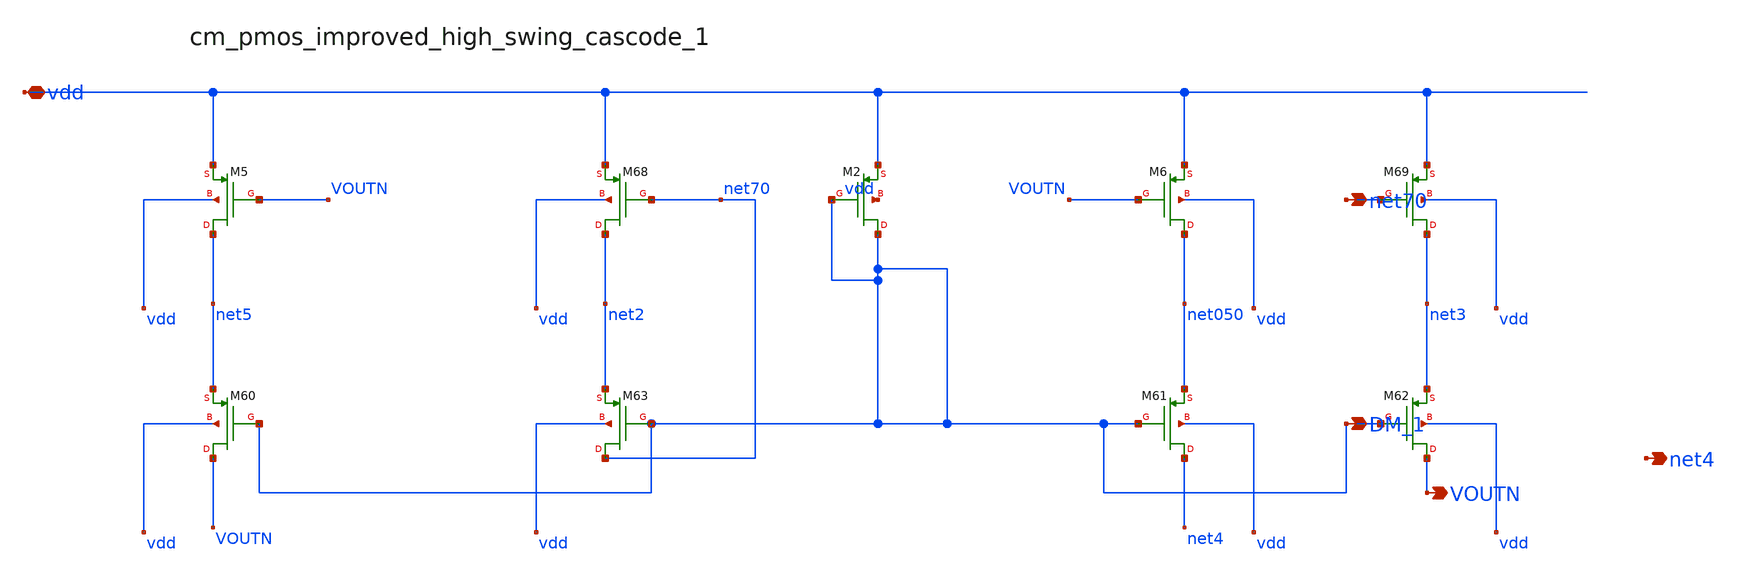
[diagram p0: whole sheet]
** sch_path: analog-db/raw/amp_016_song_dacfc/hier/blocks/cm_pmos_improved_high_swing_cascode_1.sch
**.subckt cm_pmos_improved_high_swing_cascode_1 vdd VOUTN net70 DM_1 net4
*.iopin vdd
*.opin VOUTN
*.opin net70
*.opin DM_1
*.opin net4
XM2 DM_1 DM_1 vdd vdd sg13_lv_pmos w=x_dut_xm2_w l=x_dut_xm2_l ng=1 m=x_dut_xm2_m
XM5 net5 VOUTN vdd vdd sg13_lv_pmos w=x_dut_xm5_w l=x_dut_xm5_l ng=1 m=x_dut_xm5_m
XM6 net050 VOUTN vdd vdd sg13_lv_pmos w=x_dut_xm6_w l=x_dut_xm6_l ng=1 m=x_dut_xm6_m
XM60 VOUTN DM_1 net5 vdd sg13_lv_pmos w=x_dut_xm60_w l=x_dut_xm60_l ng=1 m=x_dut_xm60_m
XM61 net4 DM_1 net050 vdd sg13_lv_pmos w=x_dut_xm61_w l=x_dut_xm61_l ng=1 m=x_dut_xm61_m
XM62 VOUTN DM_1 net3 vdd sg13_lv_pmos w=x_dut_xm62_w l=x_dut_xm62_l ng=1 m=x_dut_xm62_m
XM63 net70 DM_1 net2 vdd sg13_lv_pmos w=x_dut_xm63_w l=x_dut_xm63_l ng=1 m=x_dut_xm63_m
XM68 net2 net70 vdd vdd sg13_lv_pmos w=x_dut_xm68_w l=x_dut_xm68_l ng=1 m=x_dut_xm68_m
XM69 net3 net70 vdd vdd sg13_lv_pmos w=x_dut_xm69_w l=x_dut_xm69_l ng=1 m=x_dut_xm69_m
**.ends
.end
